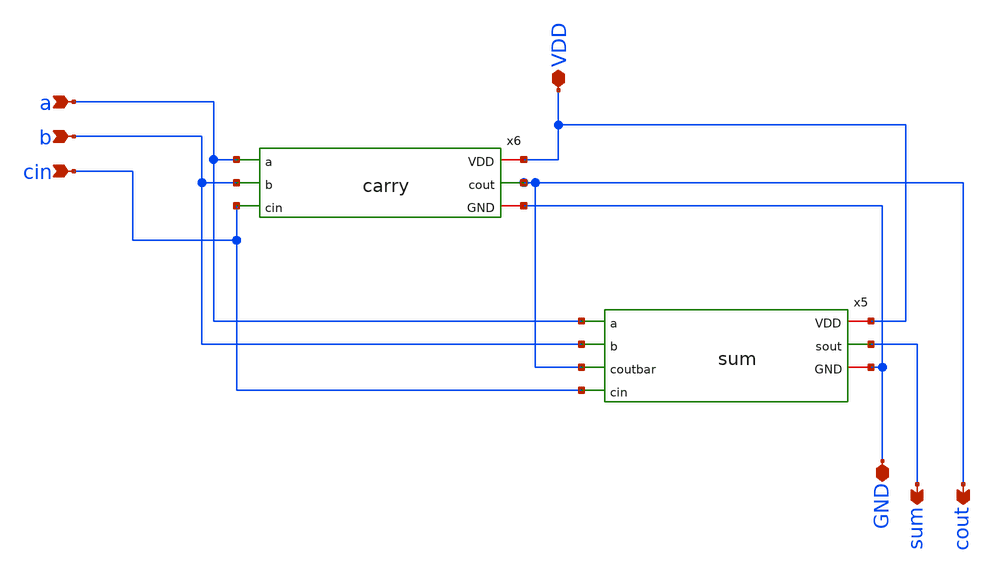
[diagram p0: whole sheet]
** sch_path: assignments/assignment8/rca1.sch
**.subckt rca1 VDD GND a sum b cin cout
*.iopin VDD
*.iopin GND
*.ipin a
*.opin sum
*.ipin b
*.ipin cin
*.opin cout
x5 VDD a b cout cin sum GND sum
x6 VDD a b cin cout GND carry
**.ends
.end
